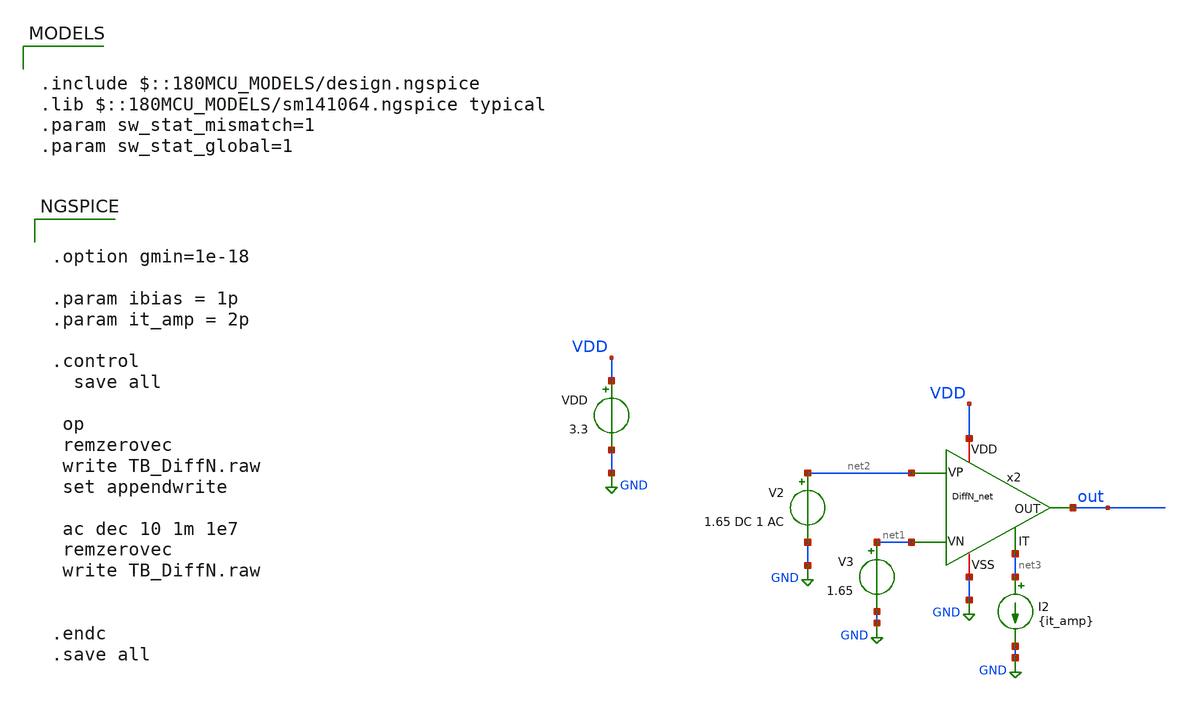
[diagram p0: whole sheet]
** sch_path: TIA/xschem/PseudoResistor/TB_DiffN.sch
**.subckt TB_DiffN
VDD VDD GND 3.3
x2 net1 net2 out net3 VDD GND DiffN_net
V2 net2 GND 1.65 DC 1 AC
V3 net1 GND 1.65
I2 net3 GND {it_amp}
**** begin user architecture code

.include $::180MCU_MODELS/design.ngspice
.lib $::180MCU_MODELS/sm141064.ngspice typical
.param sw_stat_mismatch=1
.param sw_stat_global=1



.option gmin=1e-18

.param ibias = 1p
.param it_amp = 2p

.control
  save all

 op
 remzerovec
 write TB_DiffN.raw
 set appendwrite

 ac dec 10 1m 1e7
 remzerovec
 write TB_DiffN.raw


.endc
.save all


**** end user architecture code
**.ends
.GLOBAL GND
.end
